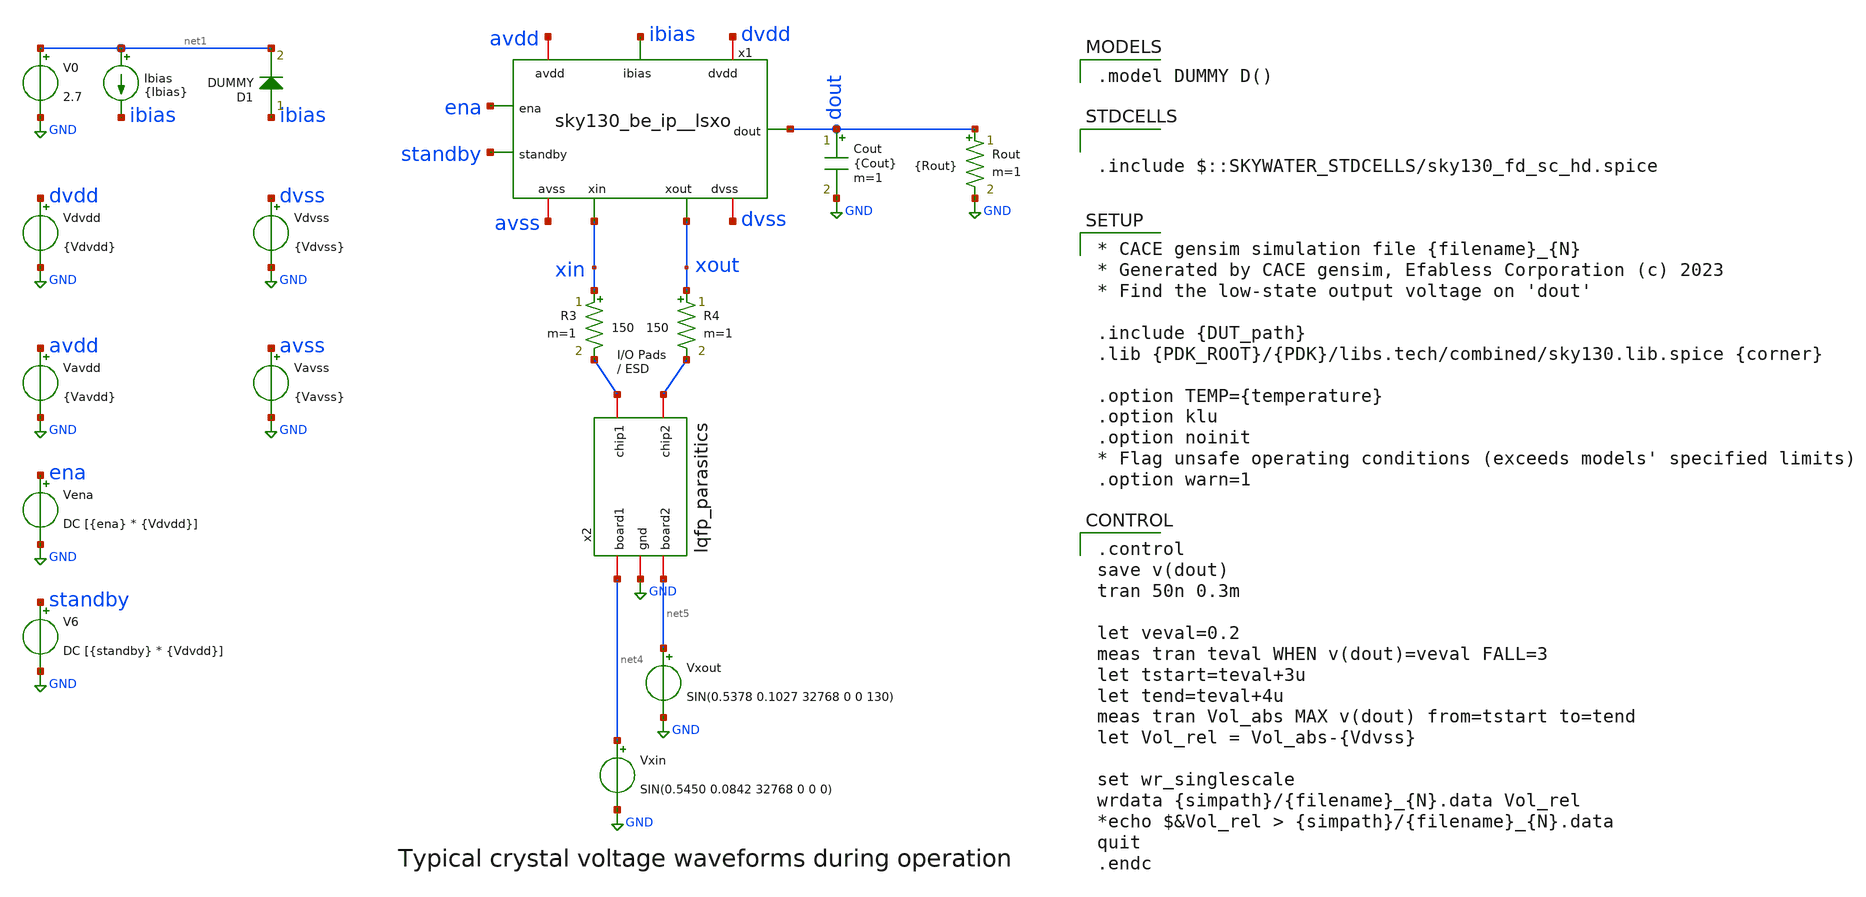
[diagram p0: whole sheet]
** sch_path: cace/templates/tb_vol.sch

.include $::SKYWATER_STDCELLS/sky130_fd_sc_hd.spice

**.subckt tb_vol
Vdvdd dvdd GND {Vdvdd}
Vavdd avdd GND {Vavdd}
Ibias net1 ibias {Ibias}
Cout dout GND {Cout} m=1
V0 net1 GND 2.7
V6 standby GND DC [{standby} * {Vdvdd}]
R3 xin net2 150 m=1
R4 xout net3 150 m=1
x2 net3 net2 GND net4 net5 lqfp_parasitics
Vena ena GND DC [{ena} * {Vdvdd}]
D1 ibias net1 DUMMY area=100
x1 avdd avss dvdd dvss ibias ena standby dout xin xout sky130_be_ip__lsxo
Vdvss dvss GND {Vdvss}
Vavss avss GND {Vavss}
Rout dout GND {Rout} m=1
Vxout net5 GND SIN(0.5378 0.1027 32768 0 0 130)
Vxin net4 GND SIN(0.5450 0.0842 32768 0 0 0)
**** begin user architecture code

.model DUMMY D()


.control
save v(dout)
tran 50n 0.3m

let veval=0.2
meas tran teval WHEN v(dout)=veval FALL=3
let tstart=teval+3u
let tend=teval+4u
meas tran Vol_abs MAX v(dout) from=tstart to=tend
let Vol_rel = Vol_abs-{Vdvss}

set wr_singlescale
wrdata {simpath}/{filename}_{N}.data Vol_rel
*echo $&Vol_rel > {simpath}/{filename}_{N}.data
quit
.endc



* CACE gensim simulation file {filename}_{N}
* Generated by CACE gensim, Efabless Corporation (c) 2023
* Find the low-state output voltage on 'dout'

.include {DUT_path}
.lib {PDK_ROOT}/{PDK}/libs.tech/combined/sky130.lib.spice {corner}

.option TEMP={temperature}
.option klu
.option noinit
* Flag unsafe operating conditions (exceeds models' specified limits)
.option warn=1


**** end user architecture code
**.ends
.GLOBAL GND
.end
